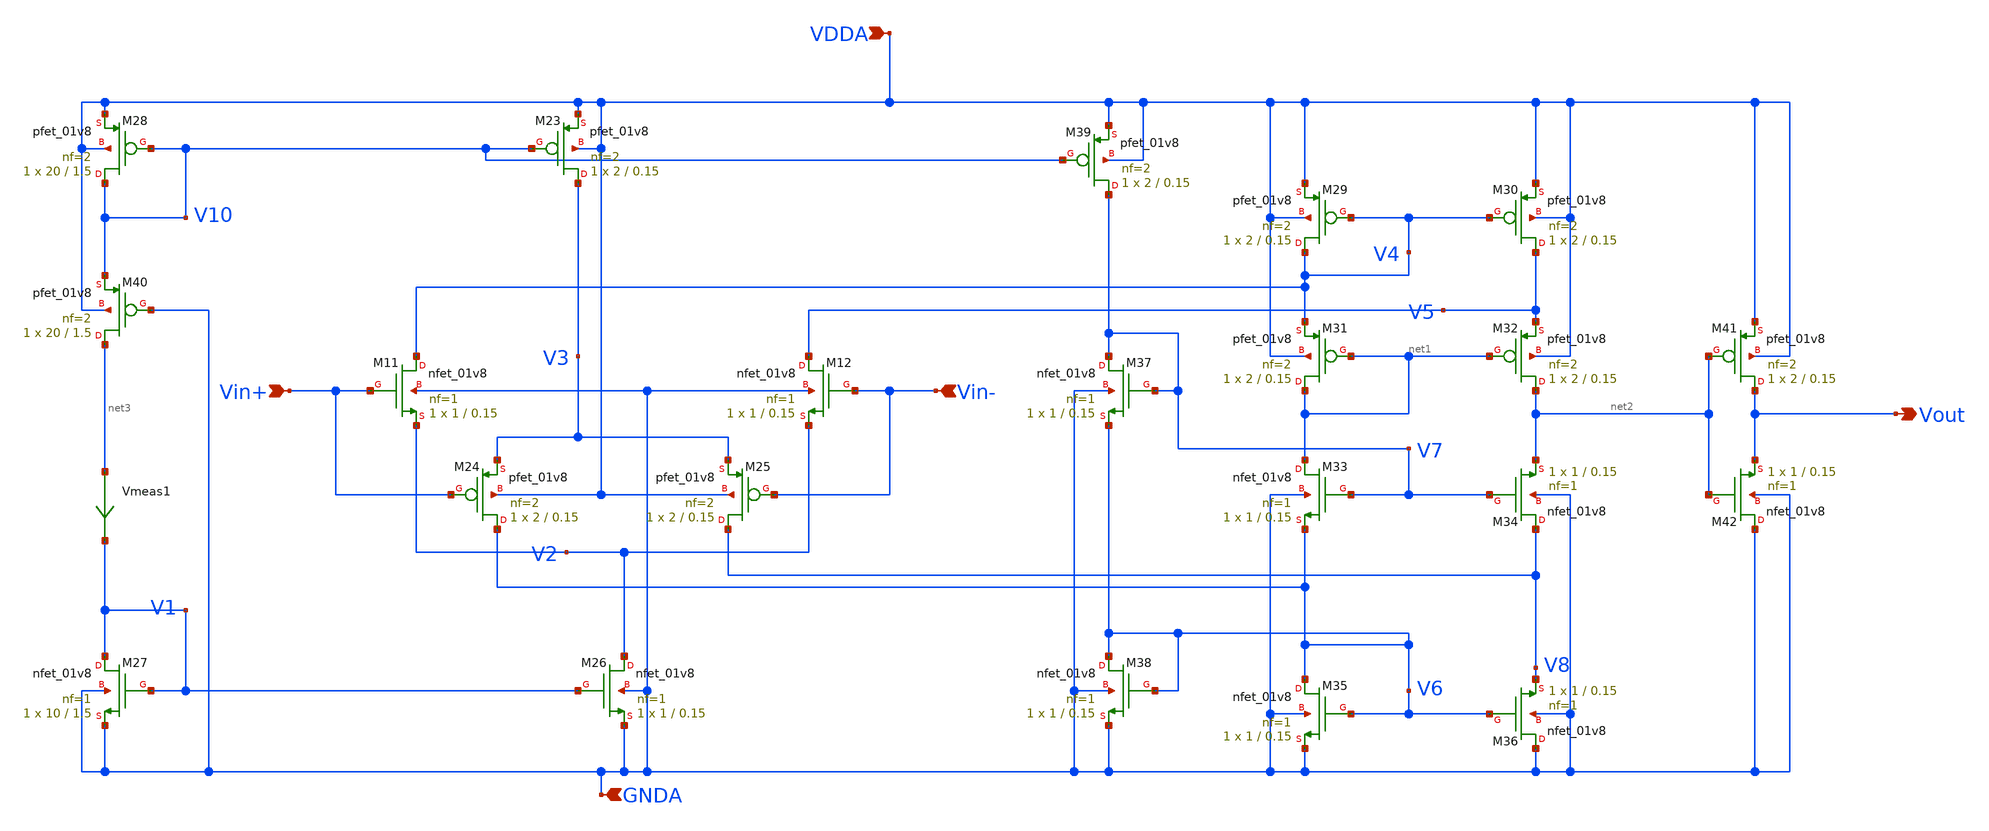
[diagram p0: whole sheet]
** sch_path: projects/pll/charge_pump/xschem_ngspice/rail_to_rail_opamp2.sch
**.subckt rail_to_rail_opamp2 VDDA Vin+ Vin- GNDA Vout
*.ipin VDDA
*.ipin Vin+
*.ipin Vin-
*.ipin GNDA
*.opin Vout
XM11 V4 Vin+ V2 GNDA sky130_fd_pr__nfet_01v8 L=0.15 W=1 nf=1 ad='int((nf+1)/2) * W/nf * 0.29' as='int((nf+2)/2) * W/nf * 0.29'
+ pd='2*int((nf+1)/2) * (W/nf + 0.29)' ps='2*int((nf+2)/2) * (W/nf + 0.29)' nrd='0.29 / W' nrs='0.29 / W'
+ sa=0 sb=0 sd=0 mult=1 m=1
XM12 V5 Vin- V2 GNDA sky130_fd_pr__nfet_01v8 L=0.15 W=1 nf=1 ad='int((nf+1)/2) * W/nf * 0.29' as='int((nf+2)/2) * W/nf * 0.29'
+ pd='2*int((nf+1)/2) * (W/nf + 0.29)' ps='2*int((nf+2)/2) * (W/nf + 0.29)' nrd='0.29 / W' nrs='0.29 / W'
+ sa=0 sb=0 sd=0 mult=1 m=1
XM23 V3 V10 VDDA VDDA sky130_fd_pr__pfet_01v8 L=0.15 W=2 nf=2 ad='int((nf+1)/2) * W/nf * 0.29' as='int((nf+2)/2) * W/nf * 0.29'
+ pd='2*int((nf+1)/2) * (W/nf + 0.29)' ps='2*int((nf+2)/2) * (W/nf + 0.29)' nrd='0.29 / W' nrs='0.29 / W'
+ sa=0 sb=0 sd=0 mult=1 m=1
XM24 V6 Vin+ V3 VDDA sky130_fd_pr__pfet_01v8 L=0.15 W=2 nf=2 ad='int((nf+1)/2) * W/nf * 0.29' as='int((nf+2)/2) * W/nf * 0.29'
+ pd='2*int((nf+1)/2) * (W/nf + 0.29)' ps='2*int((nf+2)/2) * (W/nf + 0.29)' nrd='0.29 / W' nrs='0.29 / W'
+ sa=0 sb=0 sd=0 mult=1 m=1
XM25 V8 Vin- V3 VDDA sky130_fd_pr__pfet_01v8 L=0.15 W=2 nf=2 ad='int((nf+1)/2) * W/nf * 0.29' as='int((nf+2)/2) * W/nf * 0.29'
+ pd='2*int((nf+1)/2) * (W/nf + 0.29)' ps='2*int((nf+2)/2) * (W/nf + 0.29)' nrd='0.29 / W' nrs='0.29 / W'
+ sa=0 sb=0 sd=0 mult=1 m=1
XM26 V2 V1 GNDA GNDA sky130_fd_pr__nfet_01v8 L=0.15 W=1 nf=1 ad='int((nf+1)/2) * W/nf * 0.29' as='int((nf+2)/2) * W/nf * 0.29'
+ pd='2*int((nf+1)/2) * (W/nf + 0.29)' ps='2*int((nf+2)/2) * (W/nf + 0.29)' nrd='0.29 / W' nrs='0.29 / W'
+ sa=0 sb=0 sd=0 mult=1 m=1
XM27 V1 V1 GNDA GNDA sky130_fd_pr__nfet_01v8 L=1.5 W=10 nf=1 ad='int((nf+1)/2) * W/nf * 0.29' as='int((nf+2)/2) * W/nf * 0.29'
+ pd='2*int((nf+1)/2) * (W/nf + 0.29)' ps='2*int((nf+2)/2) * (W/nf + 0.29)' nrd='0.29 / W' nrs='0.29 / W'
+ sa=0 sb=0 sd=0 mult=1 m=1
XM28 V10 V10 VDDA VDDA sky130_fd_pr__pfet_01v8 L=1.5 W=20 nf=2 ad='int((nf+1)/2) * W/nf * 0.29' as='int((nf+2)/2) * W/nf * 0.29'
+ pd='2*int((nf+1)/2) * (W/nf + 0.29)' ps='2*int((nf+2)/2) * (W/nf + 0.29)' nrd='0.29 / W' nrs='0.29 / W'
+ sa=0 sb=0 sd=0 mult=1 m=1
XM29 V4 V4 VDDA VDDA sky130_fd_pr__pfet_01v8 L=0.15 W=2 nf=2 ad='int((nf+1)/2) * W/nf * 0.29' as='int((nf+2)/2) * W/nf * 0.29'
+ pd='2*int((nf+1)/2) * (W/nf + 0.29)' ps='2*int((nf+2)/2) * (W/nf + 0.29)' nrd='0.29 / W' nrs='0.29 / W'
+ sa=0 sb=0 sd=0 mult=1 m=1
XM30 V5 V4 VDDA VDDA sky130_fd_pr__pfet_01v8 L=0.15 W=2 nf=2 ad='int((nf+1)/2) * W/nf * 0.29' as='int((nf+2)/2) * W/nf * 0.29'
+ pd='2*int((nf+1)/2) * (W/nf + 0.29)' ps='2*int((nf+2)/2) * (W/nf + 0.29)' nrd='0.29 / W' nrs='0.29 / W'
+ sa=0 sb=0 sd=0 mult=1 m=1
XM31 net1 net1 V4 VDDA sky130_fd_pr__pfet_01v8 L=0.15 W=2 nf=2 ad='int((nf+1)/2) * W/nf * 0.29' as='int((nf+2)/2) * W/nf * 0.29'
+ pd='2*int((nf+1)/2) * (W/nf + 0.29)' ps='2*int((nf+2)/2) * (W/nf + 0.29)' nrd='0.29 / W' nrs='0.29 / W'
+ sa=0 sb=0 sd=0 mult=1 m=1
XM32 net2 net1 V5 VDDA sky130_fd_pr__pfet_01v8 L=0.15 W=2 nf=2 ad='int((nf+1)/2) * W/nf * 0.29' as='int((nf+2)/2) * W/nf * 0.29'
+ pd='2*int((nf+1)/2) * (W/nf + 0.29)' ps='2*int((nf+2)/2) * (W/nf + 0.29)' nrd='0.29 / W' nrs='0.29 / W'
+ sa=0 sb=0 sd=0 mult=1 m=1
XM33 net1 V7 V6 GNDA sky130_fd_pr__nfet_01v8 L=0.15 W=1 nf=1 ad='int((nf+1)/2) * W/nf * 0.29' as='int((nf+2)/2) * W/nf * 0.29'
+ pd='2*int((nf+1)/2) * (W/nf + 0.29)' ps='2*int((nf+2)/2) * (W/nf + 0.29)' nrd='0.29 / W' nrs='0.29 / W'
+ sa=0 sb=0 sd=0 mult=1 m=1
XM34 V8 V7 net2 GNDA sky130_fd_pr__nfet_01v8 L=0.15 W=1 nf=1 ad='int((nf+1)/2) * W/nf * 0.29' as='int((nf+2)/2) * W/nf * 0.29'
+ pd='2*int((nf+1)/2) * (W/nf + 0.29)' ps='2*int((nf+2)/2) * (W/nf + 0.29)' nrd='0.29 / W' nrs='0.29 / W'
+ sa=0 sb=0 sd=0 mult=1 m=1
XM35 V6 V6 GNDA GNDA sky130_fd_pr__nfet_01v8 L=0.15 W=1 nf=1 ad='int((nf+1)/2) * W/nf * 0.29' as='int((nf+2)/2) * W/nf * 0.29'
+ pd='2*int((nf+1)/2) * (W/nf + 0.29)' ps='2*int((nf+2)/2) * (W/nf + 0.29)' nrd='0.29 / W' nrs='0.29 / W'
+ sa=0 sb=0 sd=0 mult=1 m=1
XM36 GNDA V6 V8 GNDA sky130_fd_pr__nfet_01v8 L=0.15 W=1 nf=1 ad='int((nf+1)/2) * W/nf * 0.29' as='int((nf+2)/2) * W/nf * 0.29'
+ pd='2*int((nf+1)/2) * (W/nf + 0.29)' ps='2*int((nf+2)/2) * (W/nf + 0.29)' nrd='0.29 / W' nrs='0.29 / W'
+ sa=0 sb=0 sd=0 mult=1 m=1
XM37 V7 V7 V6 GNDA sky130_fd_pr__nfet_01v8 L=0.15 W=1 nf=1 ad='int((nf+1)/2) * W/nf * 0.29' as='int((nf+2)/2) * W/nf * 0.29'
+ pd='2*int((nf+1)/2) * (W/nf + 0.29)' ps='2*int((nf+2)/2) * (W/nf + 0.29)' nrd='0.29 / W' nrs='0.29 / W'
+ sa=0 sb=0 sd=0 mult=1 m=1
XM38 V6 V6 GNDA GNDA sky130_fd_pr__nfet_01v8 L=0.15 W=1 nf=1 ad='int((nf+1)/2) * W/nf * 0.29' as='int((nf+2)/2) * W/nf * 0.29'
+ pd='2*int((nf+1)/2) * (W/nf + 0.29)' ps='2*int((nf+2)/2) * (W/nf + 0.29)' nrd='0.29 / W' nrs='0.29 / W'
+ sa=0 sb=0 sd=0 mult=1 m=1
XM39 V7 V10 VDDA VDDA sky130_fd_pr__pfet_01v8 L=0.15 W=2 nf=2 ad='int((nf+1)/2) * W/nf * 0.29' as='int((nf+2)/2) * W/nf * 0.29'
+ pd='2*int((nf+1)/2) * (W/nf + 0.29)' ps='2*int((nf+2)/2) * (W/nf + 0.29)' nrd='0.29 / W' nrs='0.29 / W'
+ sa=0 sb=0 sd=0 mult=1 m=1
XM40 net3 GNDA V10 VDDA sky130_fd_pr__pfet_01v8 L=1.5 W=20 nf=2 ad='int((nf+1)/2) * W/nf * 0.29' as='int((nf+2)/2) * W/nf * 0.29'
+ pd='2*int((nf+1)/2) * (W/nf + 0.29)' ps='2*int((nf+2)/2) * (W/nf + 0.29)' nrd='0.29 / W' nrs='0.29 / W'
+ sa=0 sb=0 sd=0 mult=1 m=1
Vmeas1 net3 V1 0
.save i(vmeas1)
XM41 Vout net2 VDDA VDDA sky130_fd_pr__pfet_01v8 L=0.15 W=2 nf=2 ad='int((nf+1)/2) * W/nf * 0.29' as='int((nf+2)/2) * W/nf * 0.29'
+ pd='2*int((nf+1)/2) * (W/nf + 0.29)' ps='2*int((nf+2)/2) * (W/nf + 0.29)' nrd='0.29 / W' nrs='0.29 / W'
+ sa=0 sb=0 sd=0 mult=1 m=1
XM42 GNDA net2 Vout GNDA sky130_fd_pr__nfet_01v8 L=0.15 W=1 nf=1 ad='int((nf+1)/2) * W/nf * 0.29' as='int((nf+2)/2) * W/nf * 0.29'
+ pd='2*int((nf+1)/2) * (W/nf + 0.29)' ps='2*int((nf+2)/2) * (W/nf + 0.29)' nrd='0.29 / W' nrs='0.29 / W'
+ sa=0 sb=0 sd=0 mult=1 m=1
**.ends
.end
